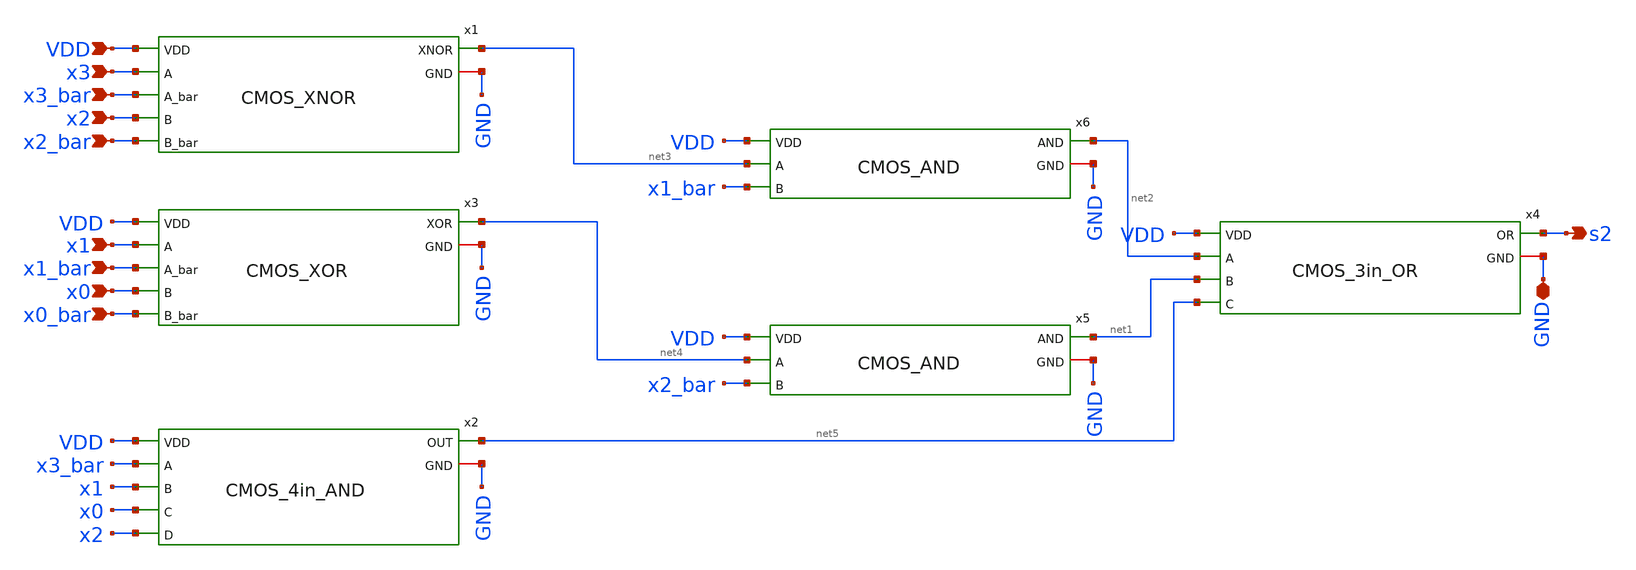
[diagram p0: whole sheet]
** sch_path: skywater_stuff/CMOS_s2_flat.sch
**.subckt CMOS_s2_flat GND x0 x0_bar x1 x1_bar x2 x2_bar x3 x3_bar s2 VDD
*.iopin GND
*.ipin x0
*.ipin x0_bar
*.ipin x1
*.ipin x1_bar
*.ipin x2
*.ipin x2_bar
*.ipin x3
*.ipin x3_bar
*.opin s2
*.ipin VDD
x4 net2 net1 net5 s2 GND VDD CMOS_3in_OR
x2 x3_bar x1 x0 x2 net5 GND VDD CMOS_4in_AND
x5 net4 x2_bar net1 GND VDD CMOS_AND
x6 net3 x1_bar net2 GND VDD CMOS_AND
x1 x3 x3_bar x2 x2_bar net3 GND VDD CMOS_XNOR
x3 x1 x1_bar x0 x0_bar net4 GND VDD CMOS_XOR
**.ends
.end
